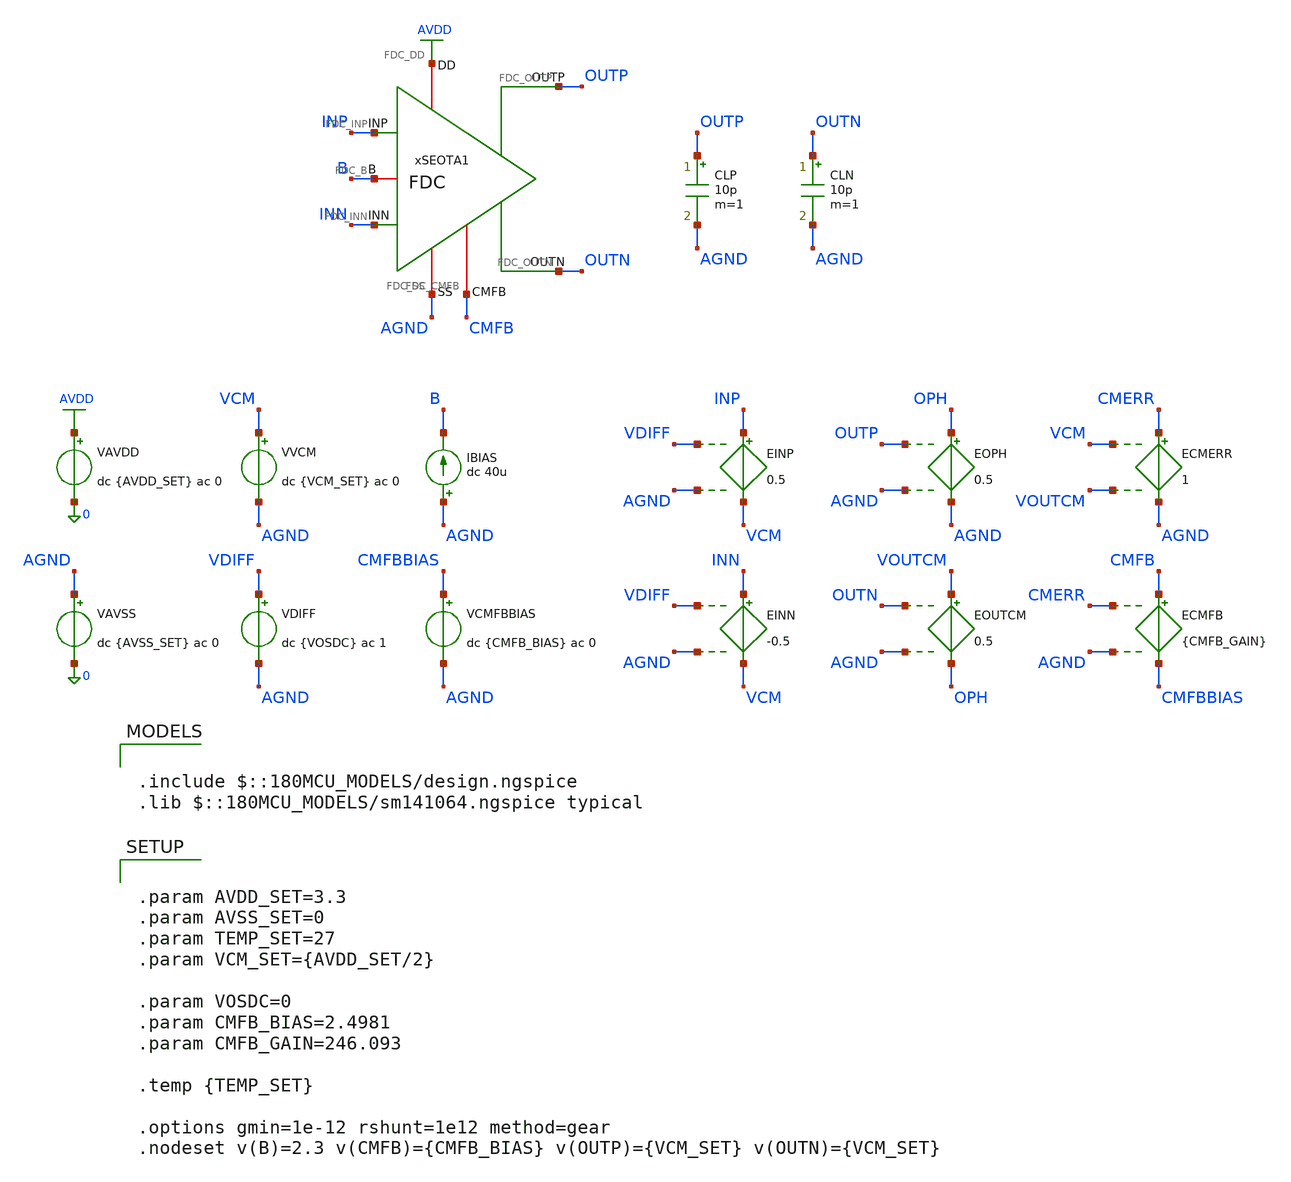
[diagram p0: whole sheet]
** sch_path: Design_Files/IC Design/Testbench/FD_OTA/FDC/Open_Loop/FDC_TB_OL_NOM.sch
**.subckt FDC_TB_OL_NOM
IBIAS AGND B dc 40u
VAVDD AVDD 0 dc {AVDD_SET} ac 0
.save i(vavdd)
CLP OUTP AGND 10p m=1
VVCM VCM AGND dc {VCM_SET} ac 0
VDIFF VDIFF AGND dc {VOSDC} ac 1
VAVSS AGND 0 dc {AVSS_SET} ac 0
.save i(vavss)
EINN INN VCM VDIFF AGND -0.5
EINP INP VCM VDIFF AGND 0.5
xSEOTA1 AVDD AGND INP INN OUTN B OUTP CMFB FDC
CLN OUTN AGND 10p m=1
VCMFBBIAS CMFBBIAS AGND dc {CMFB_BIAS} ac 0
EOUTCM VOUTCM OPH OUTN AGND 0.5
EOPH OPH AGND OUTP AGND 0.5
ECMERR CMERR AGND VCM VOUTCM 1
ECMFB CMFB CMFBBIAS CMERR AGND {CMFB_GAIN}
**** begin user architecture code

.include $::180MCU_MODELS/design.ngspice
.lib $::180MCU_MODELS/sm141064.ngspice typical



.control
destroy all
save all
set wr_vecnames
set wr_singlescale
option numdgt=15

shell mkdir -p
+ /foss/designs/ECG_Acquisition_IC/Measurement_Results/IC_Simulation/FD_OTA/FDC/NOM.Result_txt

shell rm -f
+ /foss/designs/ECG_Acquisition_IC/Measurement_Results/IC_Simulation/FD_OTA/FDC/NOM.Result_txt/NOM.ol_op.txt
shell rm -f
+ /foss/designs/ECG_Acquisition_IC/Measurement_Results/IC_Simulation/FD_OTA/FDC/NOM.Result_txt/NOM.ol_diff_ac.txt
shell rm -f
+ /foss/designs/ECG_Acquisition_IC/Measurement_Results/IC_Simulation/FD_OTA/FDC/NOM.Result_txt/NOM.ol_offset.txt
shell rm -f
+ /foss/designs/ECG_Acquisition_IC/Measurement_Results/IC_Simulation/FD_OTA/FDC/NOM.Result_txt/NOM.ol_noise.txt
shell rm -f
+ /foss/designs/ECG_Acquisition_IC/Measurement_Results/IC_Simulation/FD_OTA/FDC/NOM.Result_txt/NOM.ol_noise_integrated.txt

let avdd_run = 3.3
let vcm_run  = avdd_run/2
let vos_run  = 0

* OP
alter @VAVDD[DC] = $&avdd_run
alter @VVCM[DC]  = $&vcm_run
alter @VDIFF[DC] = $&vos_run

alter @VVCM[ACMAG]  = 0
alter @VDIFF[ACMAG] = 0
alter @VAVDD[ACMAG] = 0
alter @VAVSS[ACMAG] = 0

op

let op_vdd     = v(avdd)-v(agnd)
let op_vinp    = v(inp)-v(agnd)
let op_vinn    = v(inn)-v(agnd)
let op_vid     = op_vinp-op_vinn

let op_voutp   = v(outp)-v(agnd)
let op_voutn   = v(outn)-v(agnd)
let op_voutcm  = (op_voutp+op_voutn)/2
let op_vod     = op_voutp-op_voutn

let op_ibias   = 40e-6
let op_idd     = -vavdd#branch
let op_power   = -(v(avdd)*vavdd#branch+v(agnd)*vavss#branch)
let op_cmfb    = v(cmfb)-v(agnd)

wrdata
+ /foss/designs/ECG_Acquisition_IC/Measurement_Results/IC_Simulation/FD_OTA/FDC/NOM.Result_txt/NOM.ol_op.txt op_vdd op_vinp op_vinn op_vid op_voutp op_voutn op_voutcm op_vod op_ibias op_idd op_power op_cmfb


* Differential AC
alter @VVCM[DC]  = $&vcm_run
alter @VDIFF[DC] = $&vos_run

alter @VVCM[ACMAG]   = 0
alter @VDIFF[ACMAG]  = 1
alter @VDIFF[ACPHASE] = 0
alter @VAVDD[ACMAG]  = 0
alter @VAVSS[ACMAG]  = 0

ac dec 200 1 1G

let vid_ac  = v(inp)-v(inn)
let vod_ac  = v(outp)-v(outn)
let ad_ac   = vod_ac/vid_ac
let ad_real = real(ad_ac)
let ad_imag = imag(ad_ac)

setscale frequency

wrdata
+ /foss/designs/ECG_Acquisition_IC/Measurement_Results/IC_Simulation/FD_OTA/FDC/NOM.Result_txt/NOM.ol_diff_ac.txt ad_real ad_imag


* Offset
alter @VVCM[DC] = $&vcm_run

alter @VVCM[ACMAG]  = 0
alter @VDIFF[ACMAG] = 0
alter @VAVDD[ACMAG] = 0
alter @VAVSS[ACMAG] = 0

dc VDIFF -0.02 0.02 1e-6

let off_vdiff  = v(vdiff)-v(agnd)
let off_vinp   = v(inp)-v(agnd)
let off_vinn   = v(inn)-v(agnd)

let off_voutp  = v(outp)-v(agnd)
let off_voutn  = v(outn)-v(agnd)
let off_voutcm = (off_voutp+off_voutn)/2
let off_vod    = off_voutp-off_voutn

let off_idd    = -vavdd#branch
let off_cmfb   = v(cmfb)-v(agnd)

setscale off_vdiff

wrdata
+ /foss/designs/ECG_Acquisition_IC/Measurement_Results/IC_Simulation/FD_OTA/FDC/NOM.Result_txt/NOM.ol_offset.txt off_vinp off_vinn off_voutp off_voutn off_voutcm off_vod off_idd off_cmfb


* Integrated noise
alter @VVCM[DC]  = $&vcm_run
alter @VDIFF[DC] = $&vos_run

alter @VVCM[ACMAG]   = 0
alter @VDIFF[ACMAG]  = 1
alter @VDIFF[ACPHASE] = 0
alter @VAVDD[ACMAG]  = 0
alter @VAVSS[ACMAG]  = 0

noise v(outp,outn) VDIFF dec 100 0.05 150

setplot noise2

let input_noise_Vrms  = inoise_total
let output_noise_Vrms = onoise_total

echo f_low_Hz f_high_Hz input_noise_Vrms output_noise_Vrms >
+ /foss/designs/ECG_Acquisition_IC/Measurement_Results/IC_Simulation/FD_OTA/FDC/NOM.Result_txt/NOM.ol_noise_integrated.txt
echo 0.05 150 $&input_noise_Vrms $&output_noise_Vrms >>
+ /foss/designs/ECG_Acquisition_IC/Measurement_Results/IC_Simulation/FD_OTA/FDC/NOM.Result_txt/NOM.ol_noise_integrated.txt


* Noise density
noise v(outp,outn) VDIFF dec 100 0.01 10Meg

setplot noise3

let input_noise_VrtHz  = inoise_spectrum
let output_noise_VrtHz = onoise_spectrum

setscale frequency

wrdata
+ /foss/designs/ECG_Acquisition_IC/Measurement_Results/IC_Simulation/FD_OTA/FDC/NOM.Result_txt/NOM.ol_noise.txt input_noise_VrtHz output_noise_VrtHz

op
set altshow
show m : vgs vth vds vdsat id gm gds

.endc




.param AVDD_SET=3.3
.param AVSS_SET=0
.param TEMP_SET=27
.param VCM_SET={AVDD_SET/2}

.param VOSDC=0
.param CMFB_BIAS=2.4981
.param CMFB_GAIN=246.093

.temp {TEMP_SET}

.options gmin=1e-12 rshunt=1e12 method=gear
.nodeset v(B)=2.3 v(CMFB)={CMFB_BIAS} v(OUTP)={VCM_SET} v(OUTN)={VCM_SET}


**** end user architecture code
**.ends

* expanding   symbol:  ECG_Acquisition_IC/Design_Files/IC Design/Schematic/FD_OTA/FDC/FDC.sym # of
*+ pins=8
** sym_path: Design_Files/IC Design/Schematic/FD_OTA/FDC/FDC.sym
** sch_path: Design_Files/IC Design/Schematic/FD_OTA/FDC/FDC.sch
.subckt FDC FDC_DD FDC_SS FDC_INP FDC_INN FDC_OUTN FDC_B FDC_OUTP FDC_CMFB
*.iopin FDC_DD
*.iopin FDC_SS
*.ipin FDC_INP
*.ipin FDC_INN
*.opin FDC_OUTP
*.iopin FDC_B
*.opin FDC_OUTN
*.iopin FDC_CMFB
XM3 net4 FDC_CMFB FDC_DD FDC_DD pfet_03v3 L=2u W=1u nf=1 ad='int((nf+1)/2) * W/nf * 0.18u' as='int((nf+2)/2) * W/nf * 0.18u'
+ pd='2*int((nf+1)/2) * (W/nf + 0.18u)' ps='2*int((nf+2)/2) * (W/nf + 0.18u)' nrd='0.18u / W' nrs='0.18u / W'
+ sa=0 sb=0 sd=0 m=200
XM8 FDC_OUTP FDC_B FDC_SS FDC_SS nfet_03v3 L=0.5u W=1u nf=1 ad='int((nf+1)/2) * W/nf * 0.18u' as='int((nf+2)/2) * W/nf * 0.18u'
+ pd='2*int((nf+1)/2) * (W/nf + 0.18u)' ps='2*int((nf+2)/2) * (W/nf + 0.18u)' nrd='0.18u / W' nrs='0.18u / W'
+ sa=0 sb=0 sd=0 m=120
Rz net1 net2 2k m=1
XM5 net3 FDC_B FDC_SS FDC_SS nfet_03v3 L=2u W=1u nf=1 ad='int((nf+1)/2) * W/nf * 0.18u' as='int((nf+2)/2) * W/nf * 0.18u'
+ pd='2*int((nf+1)/2) * (W/nf + 0.18u)' ps='2*int((nf+2)/2) * (W/nf + 0.18u)' nrd='0.18u / W' nrs='0.18u / W'
+ sa=0 sb=0 sd=0 m=20
XM6 FDC_OUTP net1 FDC_DD FDC_DD pfet_03v3 L=0.5u W=1u nf=1 ad='int((nf+1)/2) * W/nf * 0.18u' as='int((nf+2)/2) * W/nf * 0.18u'
+ pd='2*int((nf+1)/2) * (W/nf + 0.18u)' ps='2*int((nf+2)/2) * (W/nf + 0.18u)' nrd='0.18u / W' nrs='0.18u / W'
+ sa=0 sb=0 sd=0 m=400
XM10 FDC_B FDC_B FDC_SS FDC_SS nfet_03v3 L=2u W=1u nf=1 ad='int((nf+1)/2) * W/nf * 0.18u' as='int((nf+2)/2) * W/nf * 0.18u'
+ pd='2*int((nf+1)/2) * (W/nf + 0.18u)' ps='2*int((nf+2)/2) * (W/nf + 0.18u)' nrd='0.18u / W' nrs='0.18u / W'
+ sa=0 sb=0 sd=0 m=50
Cc net2 FDC_OUTP 2p m=1
XM9 FDC_OUTN FDC_B FDC_SS FDC_SS nfet_03v3 L=0.5u W=1u nf=1 ad='int((nf+1)/2) * W/nf * 0.18u' as='int((nf+2)/2) * W/nf * 0.18u'
+ pd='2*int((nf+1)/2) * (W/nf + 0.18u)' ps='2*int((nf+2)/2) * (W/nf + 0.18u)' nrd='0.18u / W' nrs='0.18u / W'
+ sa=0 sb=0 sd=0 m=120
Rz1 net4 net5 2k m=1
XM7 FDC_OUTN net4 FDC_DD FDC_DD pfet_03v3 L=0.5u W=1u nf=1 ad='int((nf+1)/2) * W/nf * 0.18u' as='int((nf+2)/2) * W/nf * 0.18u'
+ pd='2*int((nf+1)/2) * (W/nf + 0.18u)' ps='2*int((nf+2)/2) * (W/nf + 0.18u)' nrd='0.18u / W' nrs='0.18u / W'
+ sa=0 sb=0 sd=0 m=400
Cc1 net5 FDC_OUTN 2p m=1
XM4 net1 FDC_CMFB FDC_DD FDC_DD pfet_03v3 L=2u W=1u nf=1 ad='int((nf+1)/2) * W/nf * 0.18u' as='int((nf+2)/2) * W/nf * 0.18u'
+ pd='2*int((nf+1)/2) * (W/nf + 0.18u)' ps='2*int((nf+2)/2) * (W/nf + 0.18u)' nrd='0.18u / W' nrs='0.18u / W'
+ sa=0 sb=0 sd=0 m=200
XM1 net4 FDC_INN net3 FDC_SS nfet_03v3 L=2u W=1u nf=1 ad='int((nf+1)/2) * W/nf * 0.18u' as='int((nf+2)/2) * W/nf * 0.18u'
+ pd='2*int((nf+1)/2) * (W/nf + 0.18u)' ps='2*int((nf+2)/2) * (W/nf + 0.18u)' nrd='0.18u / W' nrs='0.18u / W'
+ sa=0 sb=0 sd=0 m=400
XM2 net1 FDC_INP net3 FDC_SS nfet_03v3 L=2u W=1u nf=1 ad='int((nf+1)/2) * W/nf * 0.18u' as='int((nf+2)/2) * W/nf * 0.18u'
+ pd='2*int((nf+1)/2) * (W/nf + 0.18u)' ps='2*int((nf+2)/2) * (W/nf + 0.18u)' nrd='0.18u / W' nrs='0.18u / W'
+ sa=0 sb=0 sd=0 m=400
.ends

.GLOBAL AVDD
.end
